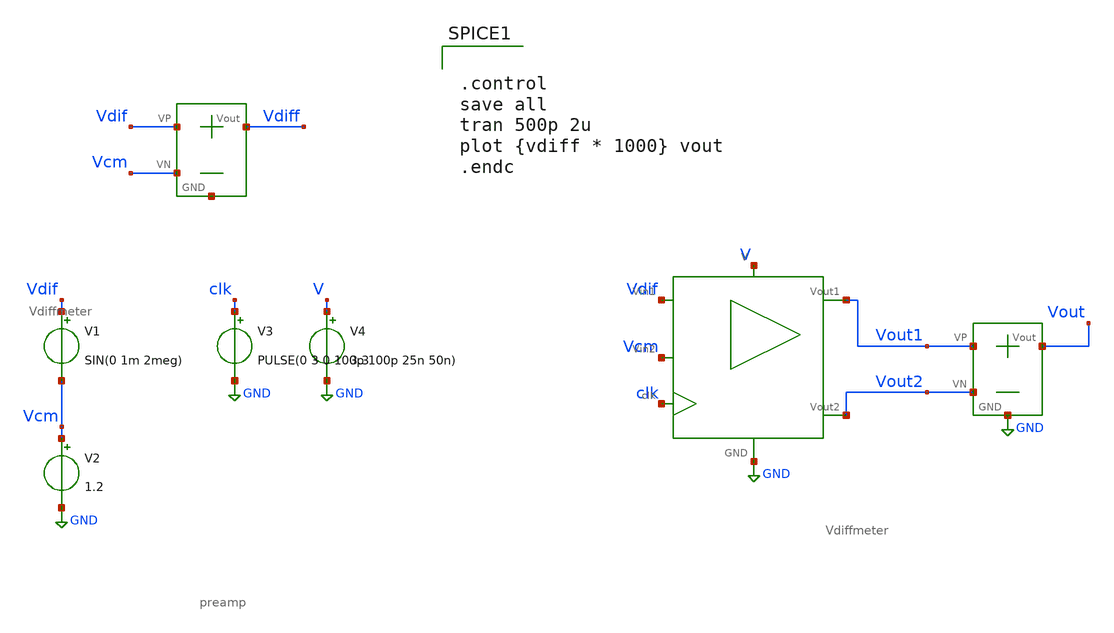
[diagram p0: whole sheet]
** sch_path: testbench/preamp_tb/sin_100k-sin_200k__tb.sch
**.subckt sin_100k-sin_200k__tb
V1 Vdif Vcm SIN(0 1m 2meg)
V2 Vcm GND 1.2
V3 clk GND PULSE(0 3 0 100p 100p 25n 50n)
V4 V GND 3.3
X1 V GND Vdif clk Vout1 Vout2 Vcm preamp
X3 Vout1 Vout2 Vout GND Vdiffmeter
X2 Vdif Vcm Vdiff net1 Vdiffmeter
**** begin user architecture code


.control
save all
tran 500p 2u
plot {vdiff * 1000} vout
.endc


.include /foss/pdks/gf180mcuC/libs.tech/ngspice/design.ngspice
.lib /foss/pdks/gf180mcuC/libs.tech/ngspice/sm141064.ngspice typical

**** end user architecture code
**.ends
.GLOBAL GND
.end
